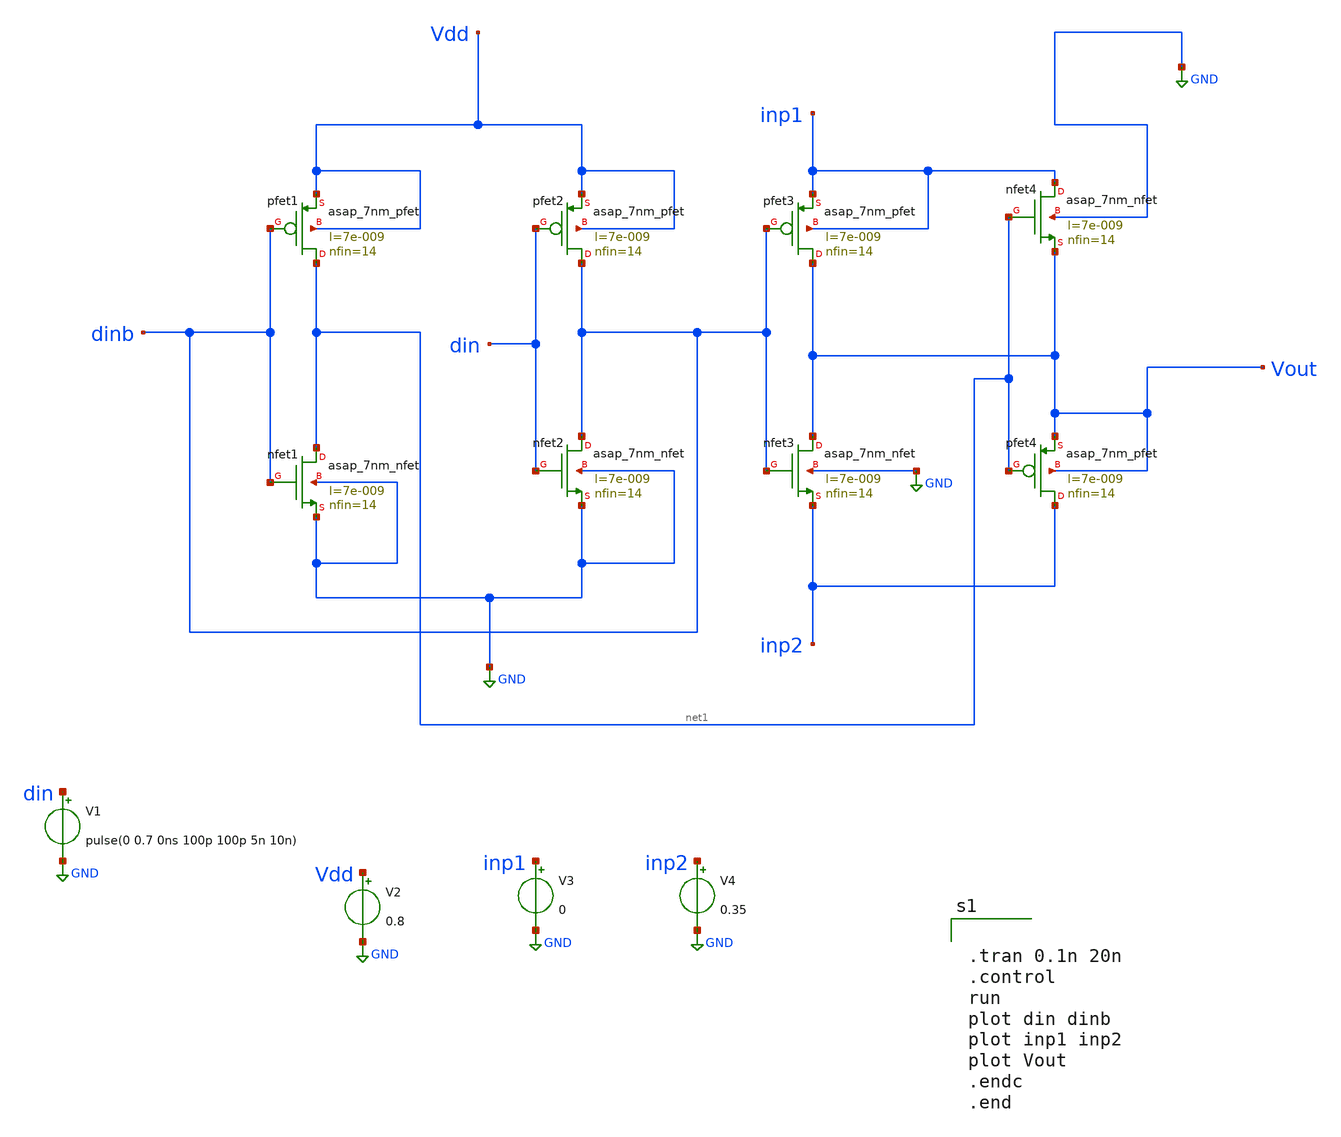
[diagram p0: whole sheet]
** sch_path: Schematics/switch.sch
**.subckt switch
Xnfet1 net1 dinb GND GND asap_7nm_nfet l=7e-009 nfin=14
Xpfet1 net1 dinb Vdd Vdd asap_7nm_pfet l=7e-009 nfin=14
Xpfet2 dinb din Vdd Vdd asap_7nm_pfet l=7e-009 nfin=14
Xnfet2 dinb din GND GND asap_7nm_nfet l=7e-009 nfin=14
Xpfet3 Vout dinb inp1 inp1 asap_7nm_pfet l=7e-009 nfin=14
Xnfet3 Vout dinb inp2 GND asap_7nm_nfet l=7e-009 nfin=14
Xpfet4 inp2 net1 Vout Vout asap_7nm_pfet l=7e-009 nfin=14
Xnfet4 inp1 net1 Vout GND asap_7nm_nfet l=7e-009 nfin=14
V1 din GND pulse(0 0.7 0ns 100p 100p 5n 10n)
V2 Vdd GND 0.8
V3 inp1 GND 0
V4 inp2 GND 0.35
**** begin user architecture code


.tran 0.1n 20n
.control
run
plot din dinb
plot inp1 inp2
plot Vout
.endc
.end


**** end user architecture code
**.ends
.GLOBAL GND
.end
